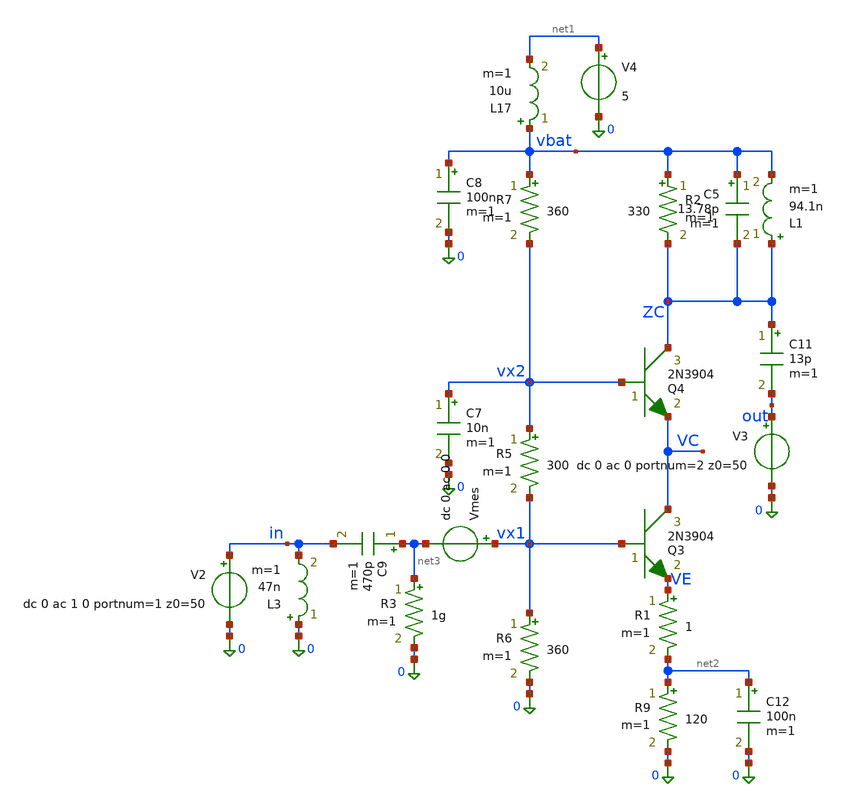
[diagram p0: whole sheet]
** sch_path: xschem_library/examples/LNA_SP.sch
**.subckt LNA_SP
V2 in 0 dc 0 ac 1 0 portnum=1 z0=50
V3 out 0 dc 0 ac 0 portnum=2 z0=50
Q3 VC vx1 VE 2N3904 area=1 m=1
R5 vx2 vx1 300 m=1
R6 vx1 0 360 m=1
Q4 ZC vx2 VC 2N3904 area=1 m=1
R7 vbat vx2 360 m=1
V4 net1 0 5
C7 vx2 0 10n m=1
C8 vbat 0 100n m=1
L17 vbat net1 10u m=1
C9 net3 in 470p m=1
C11 ZC out 13p m=1
R9 net2 0 120 m=1
C12 net2 0 100n m=1
R2 vbat ZC 330 m=1
L3 0 in 47n m=1
L1 ZC vbat 94.1n m=1
C5 vbat ZC 13.78p m=1
R1 VE net2 1 m=1
R3 net3 0 1g m=1
Vmes vx1 net3 dc 0 ac 0 0
.save i(vmes)
**** begin user architecture code


.temp 30
.option savecurrents
.save all
.control
  save all

  sp lin 1000 50meg 200meg

  let S11 = s_1_1
  let S12 = s_1_2
  let S21 = s_2_1
  let S22 = s_2_2

  let Rbase = 50
  wrs2p LNA_SP2.s2p

  remzerovec

  write LNA_SP2.raw

  *** noise figure over 50-200 MHz, 50-ohm source (V2 z0=50)
  noise V(out) V2 lin 1000 50meg 200meg
  setplot noise1

  *** per-frequency NF (NF reference T0 = 290 K, Rs = 50 ohm)
  let T0 = 290.0
  let Rsrc = 50.0
  let den = 4*boltz*T0*Rsrc
  let fvec = 1 + inoise_spectrum*inoise_spectrum/den
  let nf_db = 10*log10(fvec)
  save inoise_spectrum onoise_spectrum fvec nf_db
  write LNA_SP2_noise.raw all

  *** small-signal AC
  save all
  AC lin 1000 50Meg 200Meg
  remzerovec
  write LNA_SP2_AC.raw all
  quit 0
.endc





.model 2N3904   NPN(Is=6.734f Xti=3 Eg=1.11 Vaf=74.03 Bf=416.4 Ne=1.259                Ise=6.734f
+ Ikf=66.78m Xtb=1.5 Br=.7371 Nc=2 Isc=0 Ikr=0 Rc=1                Cjc=3.638p Mjc=.3085 Vjc=.75 Fc=.5 Cje=4.493p
+ Mje=.2593 Vje=.75                Tr=239.5n Tf=301.2p Itf=.4 Vtf=4 Xtf=2 Rb=10)

.model 2n3906   PNP(Is=455.9E-18 Xti=3 Eg=1.11 Vaf=33.6 Bf=204.7 Ise=7.558f                Ne=1.536
+ Ikf=.3287 Nk=.9957 Xtb=1.5 Var=100 Br=3.72                Isc=529.3E-18 Nc=15.51 Ikr=11.1 Rc=.8508 Cjc=10.13p
+ Mjc=.6993                Vjc=1.006 Fc=.5 Cje=10.39p Mje=.6931 Vje=.9937 Tr=10n Tf=181.2p
+                Itf=4.881m Xtf=.7939 Vtf=10 Rb=10)

.model 1N4148   D(Is=5.84n N=1.94 Rs=.7017 Ikf=44.17m Xti=3 Eg=1.11 Cjo=.95p                M=.55
+ Vj=.75 Fc=.5 Isr=11.07n Nr=2.088 Bv=100 Ibv=100u Tt=11.07n)

.MODEL SS9014 NPN (IS=2.87599e-14 BF=377.5 BR=4.79 VAF=123 VAR=11.29    IKF=1.1841 IKR=0.275423
+ ISE=4.7863e-15 ISC=1.44544e-14 NE=1.5 NC=1.5   RB=200 RBM=10 RC=5 RE=0.56 IRB=1e-5 CJE=1.7205e-11 CJC=6.2956e-12
+      VJE=0.6905907 VJC=0.4164212 MJE=0.3193434 MJC=0.2559546 TF=5.89463e-10 XTB=1.8881 XTI=3 EG=1.2415 FC=0.5
+ XCJC=0.451391 VCEO=45 ICRATING=0.1)

.MODEL QBF199 NPN (  IS  = 4.031E-16  NF  = 0.9847  ISE = 9.187E-17  NE  = 1.24  BF  = 150  IKF =
+ 0.0467  VAF = 35.8  BR  = 5  ISC = 1.00E-14  NC  = 1.5  RE  = 1  RC  = 10  CJC = 5.00E-13  CJE = 5.00E-12
+  TF  = 1.86E-10  TR  = 10E-9  ITF = 0.045  VTF = 3  XTF = 50  VJC = 0.8  MJC = 0.2  VJE = 0.6  MJE =
+ 0.4  FC  = 0.5 )


**** end user architecture code
**.ends
.end
